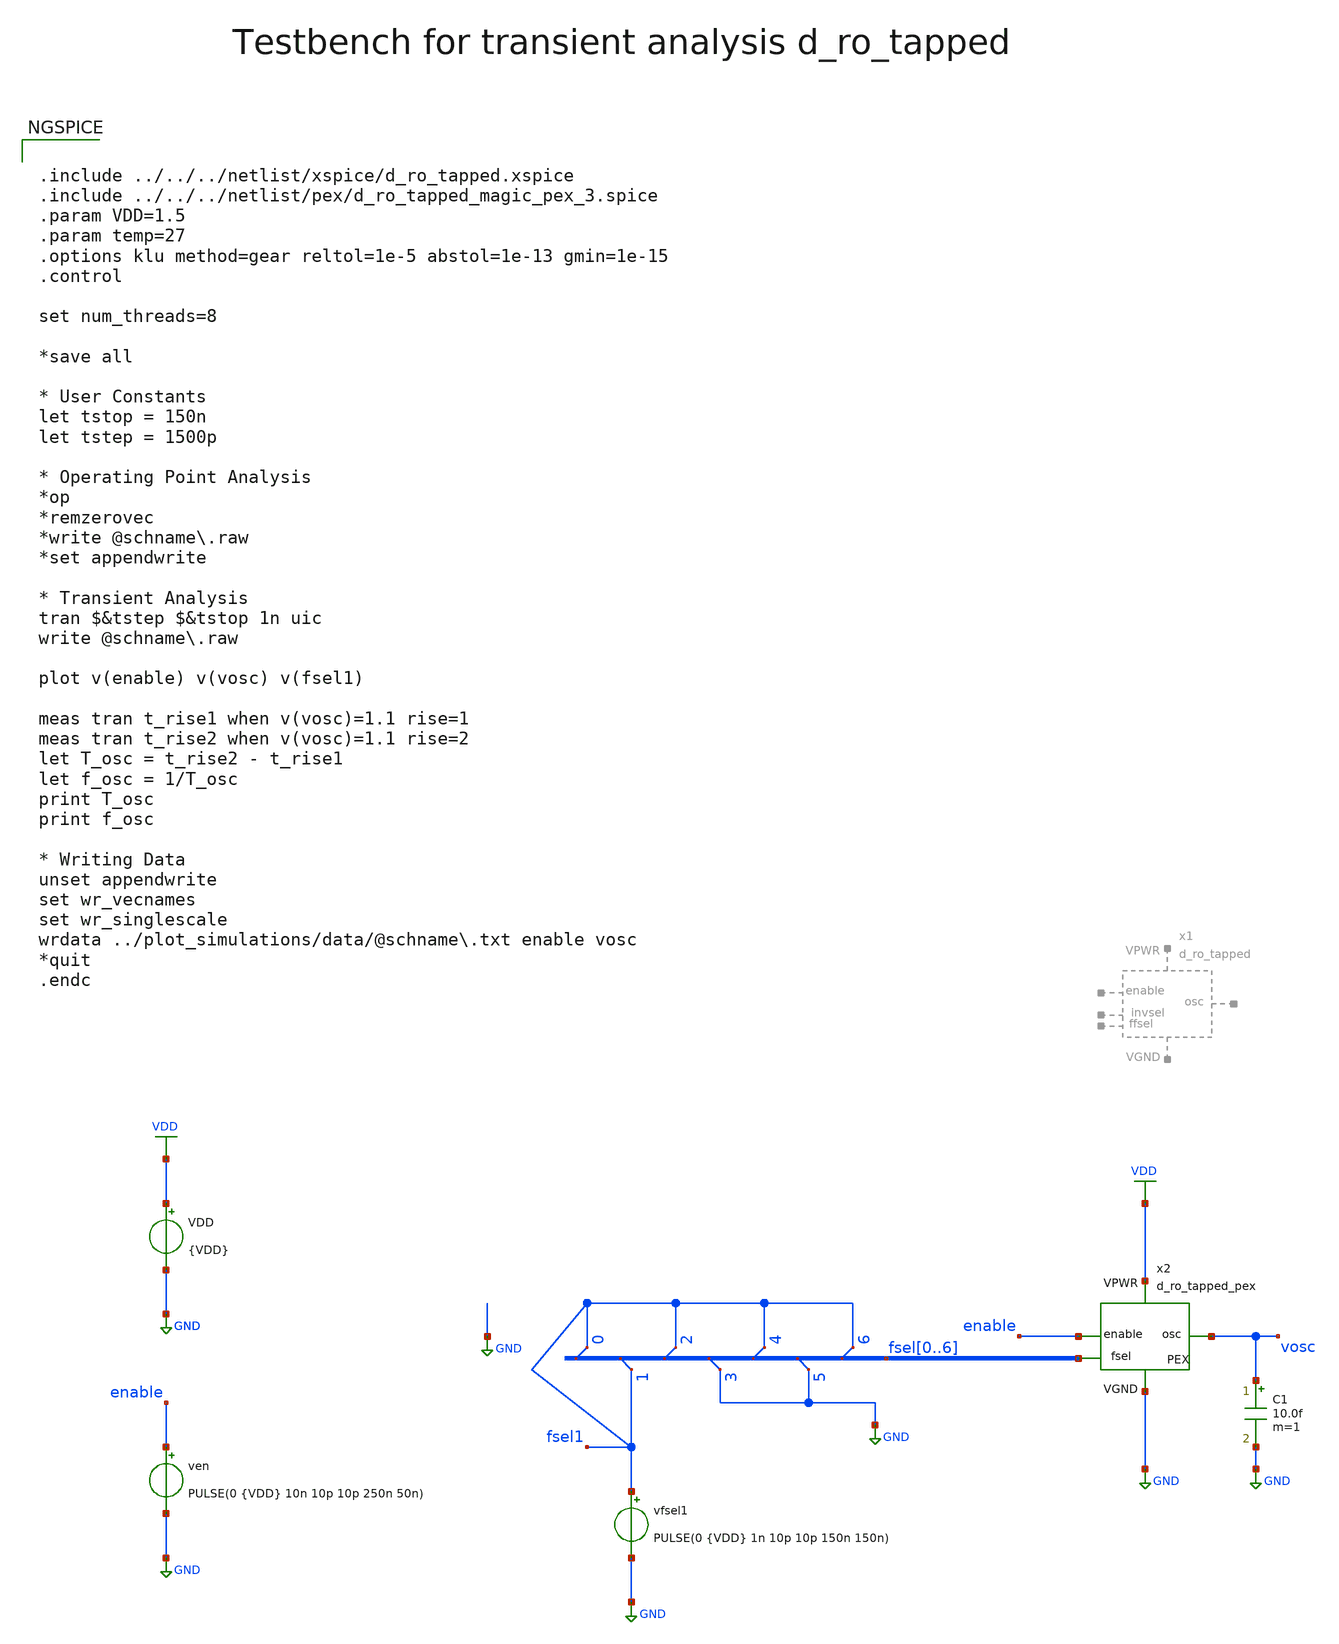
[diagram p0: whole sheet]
** sch_path: macros/heichips26_digital_project/macros/d_ro_tapped/testbenches/xschem/d_ro_tapped_tb_tran.sch
**.subckt d_ro_tapped_tb_tran
VDD VDD GND {VDD}
ven enable GND PULSE(0 {VDD} 10n 10p 10p 250n 50n)
x2 VDD GND enable vosc fsel0 fsel1 fsel2 fsel3 fsel4 fsel5 fsel6 d_ro_tapped_pex
C1 vosc GND 10.0f m=1
* tap: fsel[0..6] --> fsel6
* tap: fsel[0..6] --> fsel6
* tap: fsel[0..6] --> fsel6
* tap: fsel[0..6] --> fsel5
* tap: fsel[0..6] --> fsel6
* tap: fsel[0..6] --> fsel5
* tap: fsel[0..6] --> fsel6
vfsel1 fsel6 GND PULSE(0 {VDD} 1n 10p 10p 150n 150n)
**** begin user architecture code


.include ../../../netlist/xspice/d_ro_tapped.xspice
.include ../../../netlist/pex/d_ro_tapped_magic_pex_3.spice
.param VDD=1.5
.param temp=27
.options klu method=gear reltol=1e-5 abstol=1e-13 gmin=1e-15
.control

set num_threads=8

*save all

* User Constants
let tstop = 150n
let tstep = 1500p

* Operating Point Analysis
*op
*remzerovec
*write @schname\.raw
*set appendwrite

* Transient Analysis
tran $&tstep $&tstop 1n uic
write @schname\.raw

plot v(enable) v(vosc) v(fsel1)

meas tran t_rise1 when v(vosc)=1.1 rise=1
meas tran t_rise2 when v(vosc)=1.1 rise=2
let T_osc = t_rise2 - t_rise1
let f_osc = 1/T_osc
print T_osc
print f_osc

* Writing Data
unset appendwrite
set wr_vecnames
set wr_singlescale
wrdata ../plot_simulations/data/@schname\.txt enable vosc
*quit
.endc


.lib cornerMOSlv.lib mos_tt
.lib cornerMOShv.lib mos_tt
.lib cornerRES.lib res_typ
.lib cornerDIO.lib dio_tt

**** end user architecture code
**.ends
.GLOBAL GND
.GLOBAL VDD
.end
